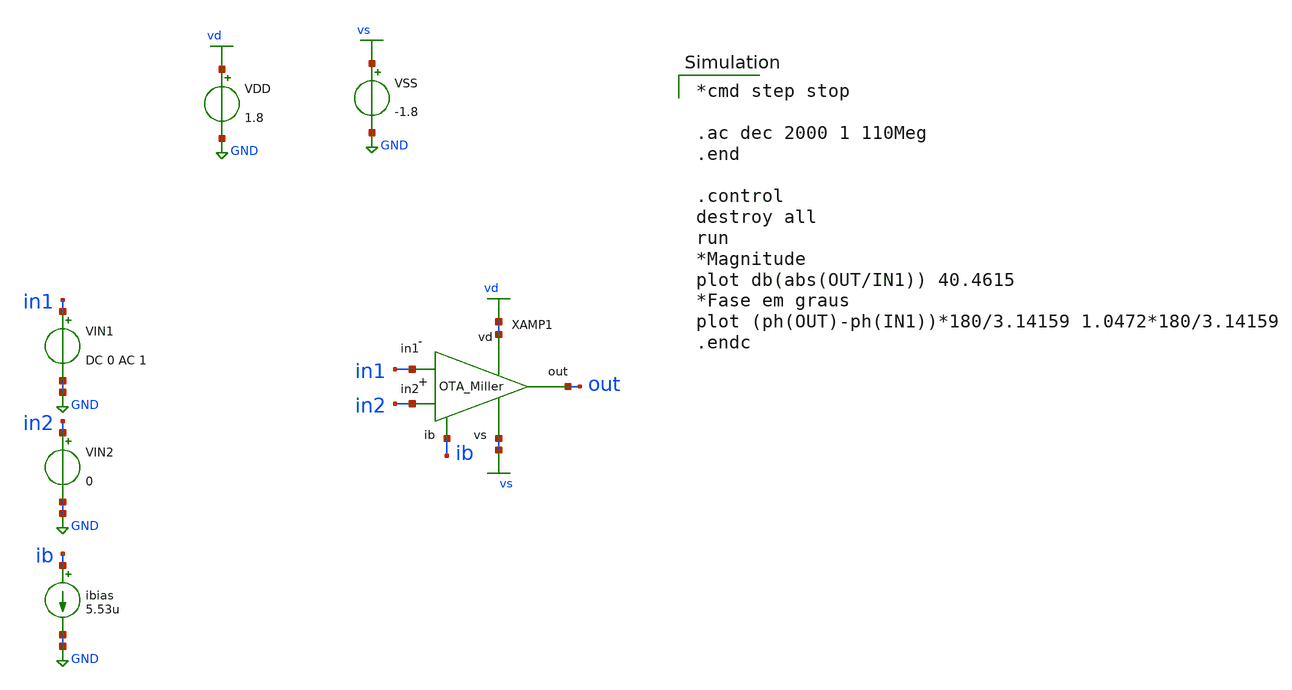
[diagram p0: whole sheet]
** sch_path: xschem/ota_tb-ac.sch
* Copyright 2020 Stefan Frederik Schippers
* Licensed under the Apache License, Version 2.0 (the "License");
* you may not use this file except in compliance with the License.
* You may obtain a copy of the License at
* https://www.apache.org/licenses/LICENSE-2.0
* Unless required by applicable law or agreed to in writing, software
* distributed under the License is distributed on an "AS IS" BASIS,
* WITHOUT WARRANTIES OR CONDITIONS OF ANY KIND, either express or implied.
* See the License for the specific language governing permissions and
* limitations under the License.
**.subckt ota_tb-ac
VIN2 in2 GND 0
VIN1 in1 GND DC 0 AC 1
ibias ib GND 5.53u
VDD vd GND 1.8
VSS vs GND -1.8
X1 vd ib out in2 in1 vs ota
**** begin user architecture code

*cmd step stop

.ac dec 2000 1 110Meg
.end

.control
destroy all
run
*Magnitude
plot db(abs(OUT/IN1)) 40.4615
*Fase em graus
plot (ph(OUT)-ph(IN1))*180/3.14159 1.0472*180/3.14159
.endc


.lib /home/hugodg/sky130_skel/dpga-ieee-sscs-contest-main/minimal_libs/skywater-pdk-libs-sky130_fd_pr/models/sky130.lib.spice tt
*.include /home/hugodg/sky130_skel/dpga-ieee-sscs-contest-main/minimal_libs/sky130_libs/sky130_lib.spice

**** end user architecture code
**.ends

* expanding   symbol:  /home/hugodg/sky130_skel/dpga-ieee-sscs-contest-main/xschem/ota.sym # of
*+ pins=6
** sym_path: xschem/ota.sym
** sch_path: xschem/ota.sch
.subckt ota vd ib out in2 in1 vs
*.iopin vd
*.opin out
*.iopin vs
*.iopin ib
*.ipin in1
*.ipin in2
Cc net1 net4 0.5p m=1
XM4 net4 net3 vs vs sky130_fd_pr__nfet_01v8 L=1 W=0.861 nf=1 ad='int((nf+1)/2) * W/nf * 0.29' as='int((nf+2)/2) * W/nf * 0.29'
+ pd='2*int((nf+1)/2) * (W/nf + 0.29)' ps='2*int((nf+2)/2) * (W/nf + 0.29)' nrd='0.29 / W' nrs='0.29 / W'
+ sa=0 sb=0 sd=0 mult=1 m=1
XM7 net1 net4 vs vs sky130_fd_pr__nfet_01v8 L=1 W=8.61 nf=1 ad='int((nf+1)/2) * W/nf * 0.29' as='int((nf+2)/2) * W/nf * 0.29'
+ pd='2*int((nf+1)/2) * (W/nf + 0.29)' ps='2*int((nf+2)/2) * (W/nf + 0.29)' nrd='0.29 / W' nrs='0.29 / W'
+ sa=0 sb=0 sd=0 mult=1 m=1
XM5 ib ib vd vd sky130_fd_pr__pfet_01v8 L=1 W=5.85 nf=1 ad='int((nf+1)/2) * W/nf * 0.29' as='int((nf+2)/2) * W/nf * 0.29'
+ pd='2*int((nf+1)/2) * (W/nf + 0.29)' ps='2*int((nf+2)/2) * (W/nf + 0.29)' nrd='0.29 / W' nrs='0.29 / W'
+ sa=0 sb=0 sd=0 mult=1 m=1
XM6 net2 ib vd vd sky130_fd_pr__pfet_01v8 L=1 W=5.85 nf=1 ad='int((nf+1)/2) * W/nf * 0.29' as='int((nf+2)/2) * W/nf * 0.29'
+ pd='2*int((nf+1)/2) * (W/nf + 0.29)' ps='2*int((nf+2)/2) * (W/nf + 0.29)' nrd='0.29 / W' nrs='0.29 / W'
+ sa=0 sb=0 sd=0 mult=1 m=1
XM8 net1 ib vd vd sky130_fd_pr__pfet_01v8 L=1 W=29.3 nf=1 ad='int((nf+1)/2) * W/nf * 0.29' as='int((nf+2)/2) * W/nf * 0.29'
+ pd='2*int((nf+1)/2) * (W/nf + 0.29)' ps='2*int((nf+2)/2) * (W/nf + 0.29)' nrd='0.29 / W' nrs='0.29 / W'
+ sa=0 sb=0 sd=0 mult=1 m=1
XM10 out ib vd vd sky130_fd_pr__pfet_01v8 L=1 W=5.85 nf=1 ad='int((nf+1)/2) * W/nf * 0.29' as='int((nf+2)/2) * W/nf * 0.29'
+ pd='2*int((nf+1)/2) * (W/nf + 0.29)' ps='2*int((nf+2)/2) * (W/nf + 0.29)' nrd='0.29 / W' nrs='0.29 / W'
+ sa=0 sb=0 sd=0 mult=1 m=1
XM9 vs net1 out out sky130_fd_pr__pfet_01v8 L=1 W=5.85 nf=1 ad='int((nf+1)/2) * W/nf * 0.29' as='int((nf+2)/2) * W/nf * 0.29'
+ pd='2*int((nf+1)/2) * (W/nf + 0.29)' ps='2*int((nf+2)/2) * (W/nf + 0.29)' nrd='0.29 / W' nrs='0.29 / W'
+ sa=0 sb=0 sd=0 mult=1 m=1
XM1 net3 in1 net2 net2 sky130_fd_pr__pfet_01v8 L=1 W=2.93 nf=1 ad='int((nf+1)/2) * W/nf * 0.29' as='int((nf+2)/2) * W/nf * 0.29'
+ pd='2*int((nf+1)/2) * (W/nf + 0.29)' ps='2*int((nf+2)/2) * (W/nf + 0.29)' nrd='0.29 / W' nrs='0.29 / W'
+ sa=0 sb=0 sd=0 mult=1 m=1
XM2 net4 in2 net2 net2 sky130_fd_pr__pfet_01v8 L=1 W=2.93 nf=1 ad='int((nf+1)/2) * W/nf * 0.29' as='int((nf+2)/2) * W/nf * 0.29'
+ pd='2*int((nf+1)/2) * (W/nf + 0.29)' ps='2*int((nf+2)/2) * (W/nf + 0.29)' nrd='0.29 / W' nrs='0.29 / W'
+ sa=0 sb=0 sd=0 mult=1 m=1
XM3 net3 net3 vs vs sky130_fd_pr__nfet_01v8 L=1 W=0.861 nf=1 ad='int((nf+1)/2) * W/nf * 0.29' as='int((nf+2)/2) * W/nf * 0.29'
+ pd='2*int((nf+1)/2) * (W/nf + 0.29)' ps='2*int((nf+2)/2) * (W/nf + 0.29)' nrd='0.29 / W' nrs='0.29 / W'
+ sa=0 sb=0 sd=0 mult=1 m=1
.ends

.GLOBAL GND
.GLOBAL vd
.GLOBAL vs
.end
